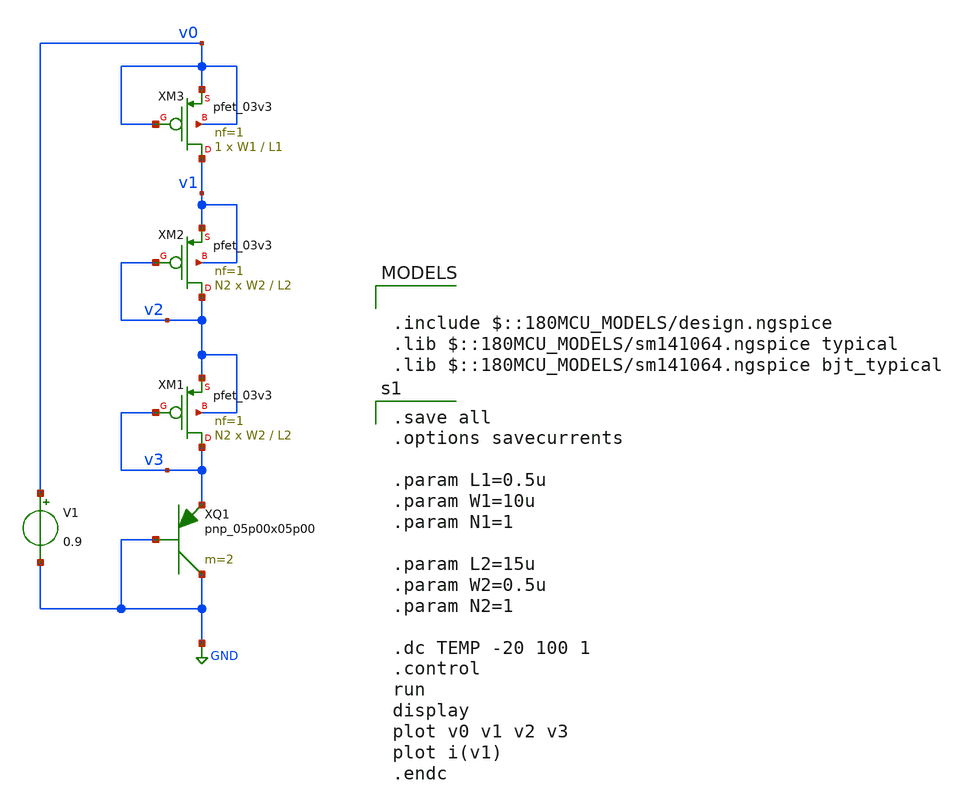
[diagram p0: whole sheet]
** sch_path: GF180/xschem/cmos_vref/Y.Ji_JSSC2019/s2_ztat.sch
**.subckt s2_ztat
XQ1 GND GND v3 pnp_05p00x05p00 m=2
V1 v0 GND 0.9
XM3 v1 v0 v0 v0 pfet_03v3 L=L1 W=W1 nf=1 ad='int((nf+1)/2) * W/nf * 0.18u' as='int((nf+2)/2) * W/nf * 0.18u'
+ pd='2*int((nf+1)/2) * (W/nf + 0.18u)' ps='2*int((nf+2)/2) * (W/nf + 0.18u)' nrd='0.18u / W' nrs='0.18u / W'
+ sa=0 sb=0 sd=0 m=1
XM2 v2 v2 v1 v1 pfet_03v3 L=L2 W=W2 nf=1 ad='int((nf+1)/2) * W/nf * 0.18u' as='int((nf+2)/2) * W/nf * 0.18u'
+ pd='2*int((nf+1)/2) * (W/nf + 0.18u)' ps='2*int((nf+2)/2) * (W/nf + 0.18u)' nrd='0.18u / W' nrs='0.18u / W'
+ sa=0 sb=0 sd=0 m=N2
XM1 v3 v3 v2 v2 pfet_03v3 L=L2 W=W2 nf=1 ad='int((nf+1)/2) * W/nf * 0.18u' as='int((nf+2)/2) * W/nf * 0.18u'
+ pd='2*int((nf+1)/2) * (W/nf + 0.18u)' ps='2*int((nf+2)/2) * (W/nf + 0.18u)' nrd='0.18u / W' nrs='0.18u / W'
+ sa=0 sb=0 sd=0 m=N2
**** begin user architecture code

.include $::180MCU_MODELS/design.ngspice
.lib $::180MCU_MODELS/sm141064.ngspice typical
.lib $::180MCU_MODELS/sm141064.ngspice bjt_typical


.save all
.options savecurrents

.param L1=0.5u
.param W1=10u
.param N1=1

.param L2=15u
.param W2=0.5u
.param N2=1

.dc TEMP -20 100 1
.control
run
display
plot v0 v1 v2 v3
plot i(v1)
.endc


**** end user architecture code
**.ends
.GLOBAL GND
.end
